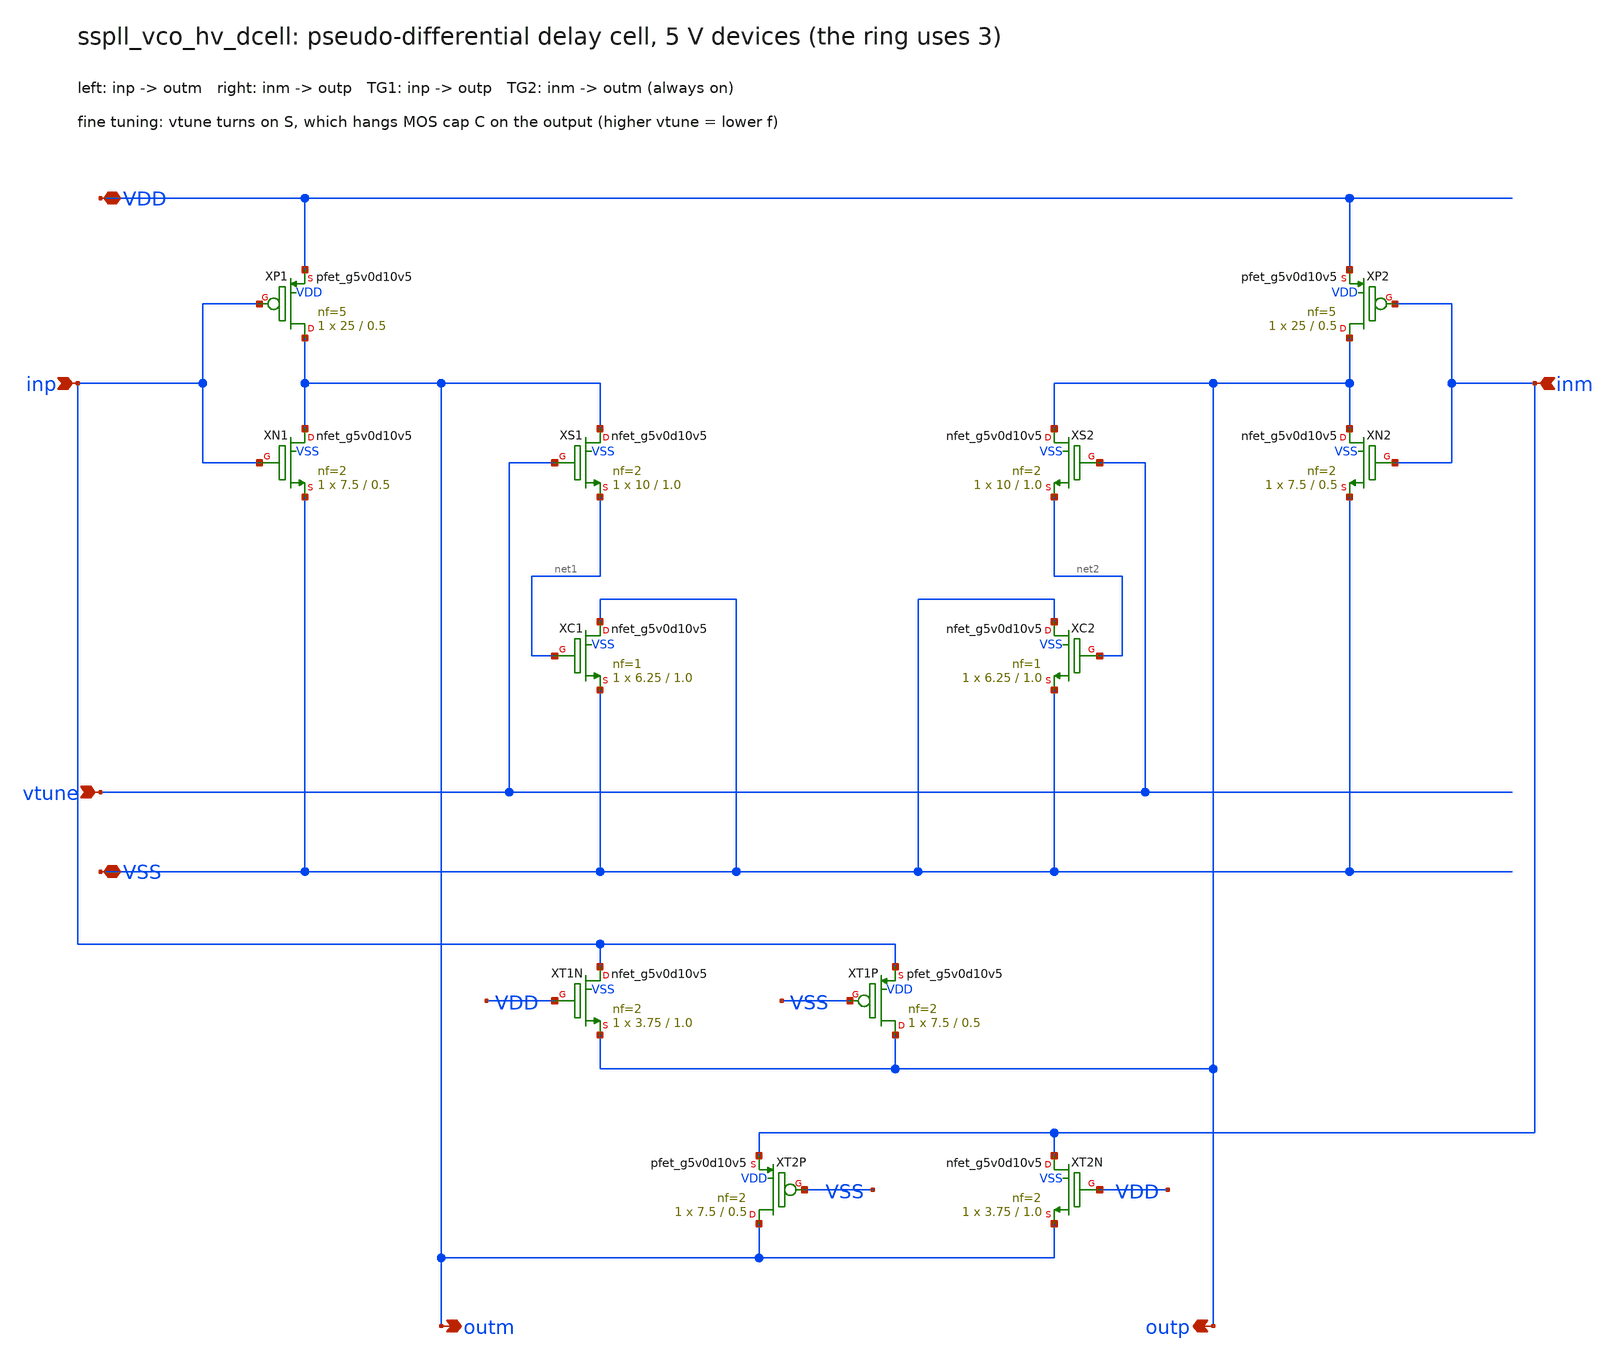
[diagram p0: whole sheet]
** sch_path: xschem/vco_hv/sspll_vco_hv_dcell.sch
**.subckt sspll_vco_hv_dcell VDD VSS vtune inp inm outm outp
*.iopin VDD
*.iopin VSS
*.ipin vtune
*.ipin inp
*.ipin inm
*.opin outm
*.opin outp
XXP1 outm inp VDD VDD sky130_fd_pr__pfet_g5v0d10v5 L=0.5 W=25 nf=5 ad='int((nf+1)/2) * W/nf * 0.29' as='int((nf+2)/2) * W/nf * 0.29'
+ pd='2*int((nf+1)/2) * (W/nf + 0.29)' ps='2*int((nf+2)/2) * (W/nf + 0.29)' nrd='0.29 / W' nrs='0.29 / W'
+ sa=0 sb=0 sd=0 mult=1 m=1
XXN1 outm inp VSS VSS sky130_fd_pr__nfet_g5v0d10v5 L=0.5 W=7.5 nf=2 ad='int((nf+1)/2) * W/nf * 0.29'
+ as='int((nf+2)/2) * W/nf * 0.29' pd='2*int((nf+1)/2) * (W/nf + 0.29)' ps='2*int((nf+2)/2) * (W/nf + 0.29)'
+ nrd='0.29 / W' nrs='0.29 / W' sa=0 sb=0 sd=0 mult=1 m=1
XXS1 outm vtune net1 VSS sky130_fd_pr__nfet_g5v0d10v5 L=1.0 W=10 nf=2 ad='int((nf+1)/2) * W/nf * 0.29'
+ as='int((nf+2)/2) * W/nf * 0.29' pd='2*int((nf+1)/2) * (W/nf + 0.29)' ps='2*int((nf+2)/2) * (W/nf + 0.29)'
+ nrd='0.29 / W' nrs='0.29 / W' sa=0 sb=0 sd=0 mult=1 m=1
XXC1 VSS net1 VSS VSS sky130_fd_pr__nfet_g5v0d10v5 L=1.0 W=6.25 nf=1 ad='int((nf+1)/2) * W/nf * 0.29'
+ as='int((nf+2)/2) * W/nf * 0.29' pd='2*int((nf+1)/2) * (W/nf + 0.29)' ps='2*int((nf+2)/2) * (W/nf + 0.29)'
+ nrd='0.29 / W' nrs='0.29 / W' sa=0 sb=0 sd=0 mult=1 m=1
XXP2 outp inm VDD VDD sky130_fd_pr__pfet_g5v0d10v5 L=0.5 W=25 nf=5 ad='int((nf+1)/2) * W/nf * 0.29' as='int((nf+2)/2) * W/nf * 0.29'
+ pd='2*int((nf+1)/2) * (W/nf + 0.29)' ps='2*int((nf+2)/2) * (W/nf + 0.29)' nrd='0.29 / W' nrs='0.29 / W'
+ sa=0 sb=0 sd=0 mult=1 m=1
XXN2 outp inm VSS VSS sky130_fd_pr__nfet_g5v0d10v5 L=0.5 W=7.5 nf=2 ad='int((nf+1)/2) * W/nf * 0.29'
+ as='int((nf+2)/2) * W/nf * 0.29' pd='2*int((nf+1)/2) * (W/nf + 0.29)' ps='2*int((nf+2)/2) * (W/nf + 0.29)'
+ nrd='0.29 / W' nrs='0.29 / W' sa=0 sb=0 sd=0 mult=1 m=1
XXS2 outp vtune net2 VSS sky130_fd_pr__nfet_g5v0d10v5 L=1.0 W=10 nf=2 ad='int((nf+1)/2) * W/nf * 0.29'
+ as='int((nf+2)/2) * W/nf * 0.29' pd='2*int((nf+1)/2) * (W/nf + 0.29)' ps='2*int((nf+2)/2) * (W/nf + 0.29)'
+ nrd='0.29 / W' nrs='0.29 / W' sa=0 sb=0 sd=0 mult=1 m=1
XXC2 VSS net2 VSS VSS sky130_fd_pr__nfet_g5v0d10v5 L=1.0 W=6.25 nf=1 ad='int((nf+1)/2) * W/nf * 0.29'
+ as='int((nf+2)/2) * W/nf * 0.29' pd='2*int((nf+1)/2) * (W/nf + 0.29)' ps='2*int((nf+2)/2) * (W/nf + 0.29)'
+ nrd='0.29 / W' nrs='0.29 / W' sa=0 sb=0 sd=0 mult=1 m=1
XXT1N inp VDD outp VSS sky130_fd_pr__nfet_g5v0d10v5 L=1.0 W=3.75 nf=2 ad='int((nf+1)/2) * W/nf * 0.29'
+ as='int((nf+2)/2) * W/nf * 0.29' pd='2*int((nf+1)/2) * (W/nf + 0.29)' ps='2*int((nf+2)/2) * (W/nf + 0.29)'
+ nrd='0.29 / W' nrs='0.29 / W' sa=0 sb=0 sd=0 mult=1 m=1
XXT1P outp VSS inp VDD sky130_fd_pr__pfet_g5v0d10v5 L=0.5 W=7.5 nf=2 ad='int((nf+1)/2) * W/nf * 0.29'
+ as='int((nf+2)/2) * W/nf * 0.29' pd='2*int((nf+1)/2) * (W/nf + 0.29)' ps='2*int((nf+2)/2) * (W/nf + 0.29)'
+ nrd='0.29 / W' nrs='0.29 / W' sa=0 sb=0 sd=0 mult=1 m=1
XXT2N inm VDD outm VSS sky130_fd_pr__nfet_g5v0d10v5 L=1.0 W=3.75 nf=2 ad='int((nf+1)/2) * W/nf * 0.29'
+ as='int((nf+2)/2) * W/nf * 0.29' pd='2*int((nf+1)/2) * (W/nf + 0.29)' ps='2*int((nf+2)/2) * (W/nf + 0.29)'
+ nrd='0.29 / W' nrs='0.29 / W' sa=0 sb=0 sd=0 mult=1 m=1
XXT2P outm VSS inm VDD sky130_fd_pr__pfet_g5v0d10v5 L=0.5 W=7.5 nf=2 ad='int((nf+1)/2) * W/nf * 0.29'
+ as='int((nf+2)/2) * W/nf * 0.29' pd='2*int((nf+1)/2) * (W/nf + 0.29)' ps='2*int((nf+2)/2) * (W/nf + 0.29)'
+ nrd='0.29 / W' nrs='0.29 / W' sa=0 sb=0 sd=0 mult=1 m=1
**.ends
.end
